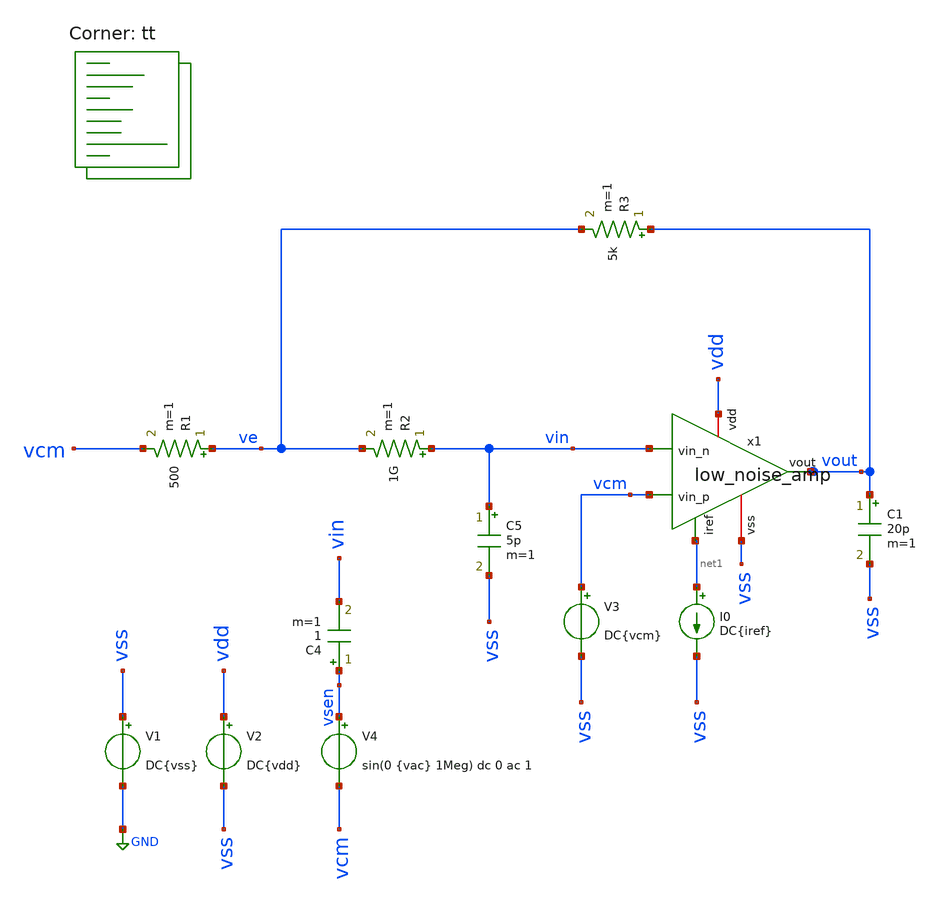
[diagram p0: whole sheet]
** sch_path: design/xschem/low_noise_amp_open_loop_tb.sch
**.subckt low_noise_amp_open_loop_tb
V1 vss GND DC{vss}
V2 vdd vss DC{vdd}
V3 vcm vss DC{vcm}
V4 vsen vcm sin(0 {vac} 1Meg) dc 0 ac 1
C4 vsen vin 1 m=1
I0 net1 vss DC{iref}
R1 ve vcm 500 m=1
R2 vin ve 1G m=1
R3 vout ve 5k m=1
C5 vin vss 5p m=1
C1 vout vss 20p m=1
x1 vdd net1 vin vcm vout vss low_noise_amp
**** begin user architecture code




* Circuit Parameters
.param iref = 100u
.param vdd  = 1.8
.param vss  = 0.0
.param vcm  = 0.8
.param vac  = 10m
.options TEMP = 65.0


* OP Parameters & Singals to save
.save all  @M.X1.XM1.msky130_fd_pr__pfet_01v8[id] @M.X1.XM1.msky130_fd_pr__pfet_01v8[vth] @M.X1.XM1.msky130_fd_pr__pfet_01v8[vgs] @M.X1.XM1.msky130_fd_pr__pfet_01v8[vds] @M.X1.XM1.msky130_fd_pr__pfet_01v8[vdsat] @M.X1.XM1.msky130_fd_pr__pfet_01v8[gm] @M.X1.XM1.msky130_fd_pr__pfet_01v8[gds]  @M.X1.XM2.msky130_fd_pr__pfet_01v8[id] @M.X1.XM2.msky130_fd_pr__pfet_01v8[vth] @M.X1.XM2.msky130_fd_pr__pfet_01v8[vgs] @M.X1.XM2.msky130_fd_pr__pfet_01v8[vds] @M.X1.XM2.msky130_fd_pr__pfet_01v8[vdsat] @M.X1.XM2.msky130_fd_pr__pfet_01v8[gm] @M.X1.XM2.msky130_fd_pr__pfet_01v8[gds]  @M.X1.XM3.msky130_fd_pr__nfet_01v8[id] @M.X1.XM3.msky130_fd_pr__nfet_01v8[vth] @M.X1.XM3.msky130_fd_pr__nfet_01v8[vgs] @M.X1.XM3.msky130_fd_pr__nfet_01v8[vds] @M.X1.XM3.msky130_fd_pr__nfet_01v8[vdsat] @M.X1.XM3.msky130_fd_pr__nfet_01v8[gm] @M.X1.XM3.msky130_fd_pr__nfet_01v8[gds]  @M.X1.XM4.msky130_fd_pr__nfet_01v8[id] @M.X1.XM4.msky130_fd_pr__nfet_01v8[vth] @M.X1.XM4.msky130_fd_pr__nfet_01v8[vgs] @M.X1.XM4.msky130_fd_pr__nfet_01v8[vds] @M.X1.XM4.msky130_fd_pr__nfet_01v8[vdsat] @M.X1.XM4.msky130_fd_pr__nfet_01v8[gm] @M.X1.XM4.msky130_fd_pr__nfet_01v8[gds]  @M.X1.XM5.msky130_fd_pr__pfet_01v8[id] @M.X1.XM5.msky130_fd_pr__pfet_01v8[vth] @M.X1.XM5.msky130_fd_pr__pfet_01v8[vgs] @M.X1.XM5.msky130_fd_pr__pfet_01v8[vds] @M.X1.XM5.msky130_fd_pr__pfet_01v8[vdsat] @M.X1.XM5.msky130_fd_pr__pfet_01v8[gm] @M.X1.XM5.msky130_fd_pr__pfet_01v8[gds]  @M.X1.XM6.msky130_fd_pr__nfet_01v8[id] @M.X1.XM6.msky130_fd_pr__nfet_01v8[vth] @M.X1.XM6.msky130_fd_pr__nfet_01v8[vgs] @M.X1.XM6.msky130_fd_pr__nfet_01v8[vds] @M.X1.XM6.msky130_fd_pr__nfet_01v8[vdsat] @M.X1.XM6.msky130_fd_pr__nfet_01v8[gm] @M.X1.XM6.msky130_fd_pr__nfet_01v8[gds]  @M.X1.XM7.msky130_fd_pr__pfet_01v8[id] @M.X1.XM7.msky130_fd_pr__pfet_01v8[vth] @M.X1.XM7.msky130_fd_pr__pfet_01v8[vgs] @M.X1.XM7.msky130_fd_pr__pfet_01v8[vds] @M.X1.XM7.msky130_fd_pr__pfet_01v8[vdsat] @M.X1.XM7.msky130_fd_pr__pfet_01v8[gm] @M.X1.XM7.msky130_fd_pr__pfet_01v8[gds]  @M.X1.XM8.msky130_fd_pr__pfet_01v8[id] @M.X1.XM8.msky130_fd_pr__pfet_01v8[vth] @M.X1.XM8.msky130_fd_pr__pfet_01v8[vgs] @M.X1.XM8.msky130_fd_pr__pfet_01v8[vds] @M.X1.XM8.msky130_fd_pr__pfet_01v8[vdsat] @M.X1.XM8.msky130_fd_pr__pfet_01v8[gm] @M.X1.XM8.msky130_fd_pr__pfet_01v8[gds]  @M.X1.XM9.msky130_fd_pr__nfet_01v8[id] @M.X1.XM9.msky130_fd_pr__nfet_01v8[vth] @M.X1.XM9.msky130_fd_pr__nfet_01v8[vgs] @M.X1.XM9.msky130_fd_pr__nfet_01v8[vds] @M.X1.XM9.msky130_fd_pr__nfet_01v8[vdsat] @M.X1.XM9.msky130_fd_pr__nfet_01v8[gm] @M.X1.XM9.msky130_fd_pr__nfet_01v8[gds]

*Simulation
.control

  ac dec 100 1 10G
  setplot ac1
  meas ac GBW when vdb(vout)=0
  meas ac DCG find vdb(vout) at=1
  meas ac PM find vp(vout) when vdb(vout)=0
  print PM*180/PI
  meas ac GM find vdb(vout) when vp(vout)=0
  plot vdb(vout) {vp(vout)*180/PI}
  write opamp_openloop_ac1.raw

  reset
  op
  setplot op1
  write opamp_openloop_op1.raw

.endc

.end


.lib $::SKYWATER_MODELS/sky130.lib.spice tt
**** end user architecture code
**.ends
.GLOBAL GND
.end
